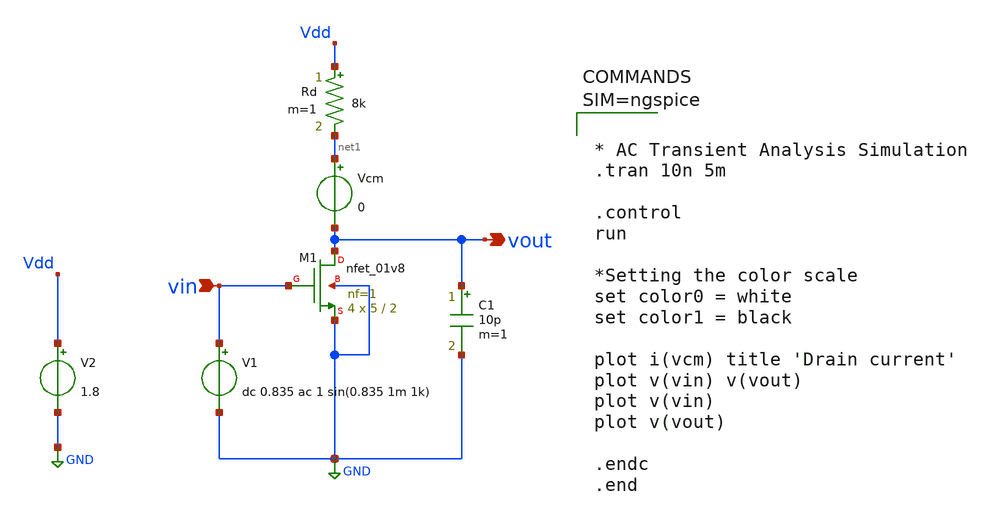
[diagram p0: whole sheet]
** sch_path: Common_Source_Restitive_Load_ckts/NMOS_CS_Amp_Res_load_AC_Transient.sch
**.subckt NMOS_CS_Amp_Res_load_AC_Transient vout vin
*.opin vout
*.ipin vin
XM1 vout vin GND GND sky130_fd_pr__nfet_01v8 L=2 W=5 nf=1 ad='int((1 + 1)/2) * 5 / 1 * 0.29' as='int((1 + 2)/2) * 5 / 1 * 0.29'
+ pd='2*int((1 + 1)/2) * (5 / 1 + 0.29)' ps='2*int((1 + 2)/2) * (5 / 1 + 0.29)' nrd='0.29 / 5 ' nrs='0.29 / 5 '
+ sa=0 sb=0 sd=0 mult=4 m=4
Rd Vdd net1 8k m=1
V1 vin GND dc 0.835 ac 1 sin(0.835 1m 1k)
V2 Vdd GND 1.8
Vcm net1 vout 0
C1 vout GND 10p m=1
**** begin user architecture code

** opencircuitdesign pdks install
.lib $::SKYWATER_MODELS/sky130.lib.spice tt




* AC Transient Analysis Simulation
.tran 10n 5m

.control
run

*Setting the color scale
set color0 = white
set color1 = black

plot i(vcm) title 'Drain current'
plot v(vin) v(vout)
plot v(vin)
plot v(vout)

.endc
.end




**** end user architecture code
**.ends
.GLOBAL GND
.end
